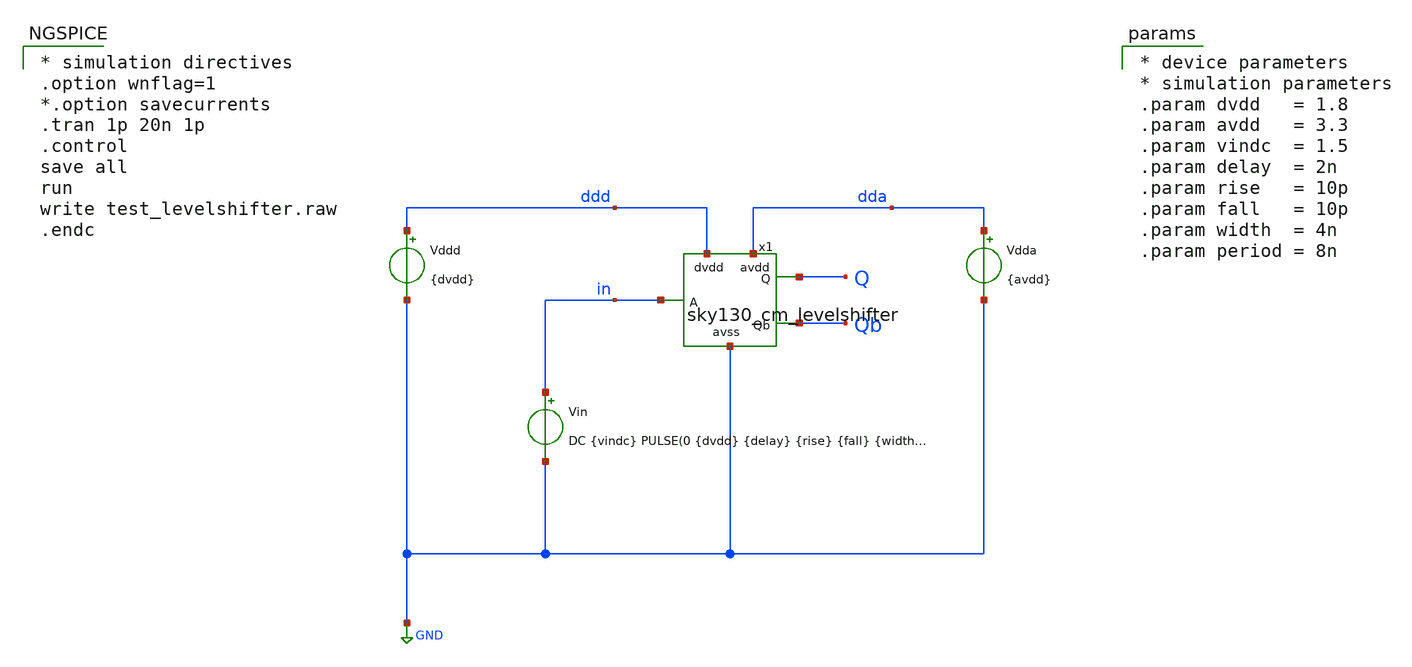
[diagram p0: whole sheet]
** sch_path: xschem/test_levelshifter.sch
**.subckt test_levelshifter
Vddd ddd GND {dvdd}
.save i(vddd)
Vdda dda GND {avdd}
.save i(vdda)
Vin in GND DC {vindc} PULSE(0 {dvdd} {delay} {rise} {fall} {width} {period})
.save i(vin)
x1 dda Q ddd Qb in GND sky130_cm_levelshifter
**** begin user architecture code

* device parameters
* simulation parameters
.param dvdd   = 1.8
.param avdd   = 3.3
.param vindc  = 1.5
.param delay  = 2n
.param rise   = 10p
.param fall   = 10p
.param width  = 4n
.param period = 8n


** opencircuitdesign pdks install
.lib $::SKYWATER_MODELS/sky130.lib.spice ff



* simulation directives
.option wnflag=1
*.option savecurrents
.tran 1p 20n 1p
.control
save all
run
write test_levelshifter.raw
.endc


**** end user architecture code
**.ends

* expanding   symbol:  xschem/sky130_cm_levelshifter.sym # of pins=6
** sym_path: xschem/sky130_cm_levelshifter.sym
** sch_path: xschem/sky130_cm_levelshifter.sch
.subckt sky130_cm_levelshifter avdd Q dvdd Qb A avss
*.iopin avss
*.iopin avdd
*.iopin A
*.iopin dvdd
*.iopin Qb
*.iopin Q
XMnl1 Q ab avss avss sky130_fd_pr__nfet_g5v0d10v5 L=0.5 W=6 nf=1 ad='int((1 + 1)/2) * 6 / 1 * 0.29' as='int((1 + 2)/2) * 6 / 1 * 0.29'
+ pd='2*int((1 + 1)/2) * (6 / 1 + 0.29)' ps='2*int((1 + 2)/2) * (6 / 1 + 0.29)' nrd='0.29 / 6 ' nrs='0.29 / 6 '
+ sa=0 sb=0 sd=0 mult=1 m=1
XMnl2 Qb abb avss avss sky130_fd_pr__nfet_g5v0d10v5 L=0.5 W=6 nf=1 ad='int((1 + 1)/2) * 6 / 1 * 0.29'
+ as='int((1 + 2)/2) * 6 / 1 * 0.29' pd='2*int((1 + 1)/2) * (6 / 1 + 0.29)' ps='2*int((1 + 2)/2) * (6 / 1 + 0.29)'
+ nrd='0.29 / 6 ' nrs='0.29 / 6 ' sa=0 sb=0 sd=0 mult=1 m=1
XMpl1 Q Qb avdd avdd sky130_fd_pr__pfet_g5v0d10v5 L=0.5 W=2 nf=1 ad='int((1 + 1)/2) * 2 / 1 * 0.29' as='int((1 + 2)/2) * 2 / 1 * 0.29'
+ pd='2*int((1 + 1)/2) * (2 / 1 + 0.29)' ps='2*int((1 + 2)/2) * (2 / 1 + 0.29)' nrd='0.29 / 2 ' nrs='0.29 / 2 '
+ sa=0 sb=0 sd=0 mult=1 m=1
XMpl2 Qb Q avdd avdd sky130_fd_pr__pfet_g5v0d10v5 L=0.5 W=2 nf=1 ad='int((1 + 1)/2) * 2 / 1 * 0.29' as='int((1 + 2)/2) * 2 / 1 * 0.29'
+ pd='2*int((1 + 1)/2) * (2 / 1 + 0.29)' ps='2*int((1 + 2)/2) * (2 / 1 + 0.29)' nrd='0.29 / 2 ' nrs='0.29 / 2 '
+ sa=0 sb=0 sd=0 mult=1 m=1
XMn1 ab A avss avss sky130_fd_pr__nfet_01v8 L=0.15 W=1 nf=1 ad='int((1 + 1)/2) * 1 / 1 * 0.29' as='int((1 + 2)/2) * 1 / 1 * 0.29'
+ pd='2*int((1 + 1)/2) * (1 / 1 + 0.29)' ps='2*int((1 + 2)/2) * (1 / 1 + 0.29)' nrd='0.29 / 1 ' nrs='0.29 / 1 '
+ sa=0 sb=0 sd=0 mult=1 m=1
XMp1 ab A dvdd dvdd sky130_fd_pr__pfet_01v8 L=0.15 W=2 nf=1 ad='int((nf+1)/2) * W/nf * 0.29' as='int((nf+2)/2) * W/nf * 0.29'
+ pd='2*int((nf+1)/2) * (W/nf + 0.29)' ps='2*int((nf+2)/2) * (W/nf + 0.29)' nrd='0.29 / W' nrs='0.29 / W'
+ sa=0 sb=0 sd=0 mult=1 m=1
XMn2 abb ab avss avss sky130_fd_pr__nfet_01v8 L=0.15 W=1 nf=1 ad='int((1 + 1)/2) * 1 / 1 * 0.29' as='int((1 + 2)/2) * 1 / 1 * 0.29'
+ pd='2*int((1 + 1)/2) * (1 / 1 + 0.29)' ps='2*int((1 + 2)/2) * (1 / 1 + 0.29)' nrd='0.29 / 1 ' nrs='0.29 / 1 '
+ sa=0 sb=0 sd=0 mult=1 m=1
XMp2 abb ab dvdd dvdd sky130_fd_pr__pfet_01v8 L=0.15 W=2 nf=1 ad='int((nf+1)/2) * W/nf * 0.29' as='int((nf+2)/2) * W/nf * 0.29'
+ pd='2*int((nf+1)/2) * (W/nf + 0.29)' ps='2*int((nf+2)/2) * (W/nf + 0.29)' nrd='0.29 / W' nrs='0.29 / W'
+ sa=0 sb=0 sd=0 mult=1 m=1
.ends

.GLOBAL GND
.end
